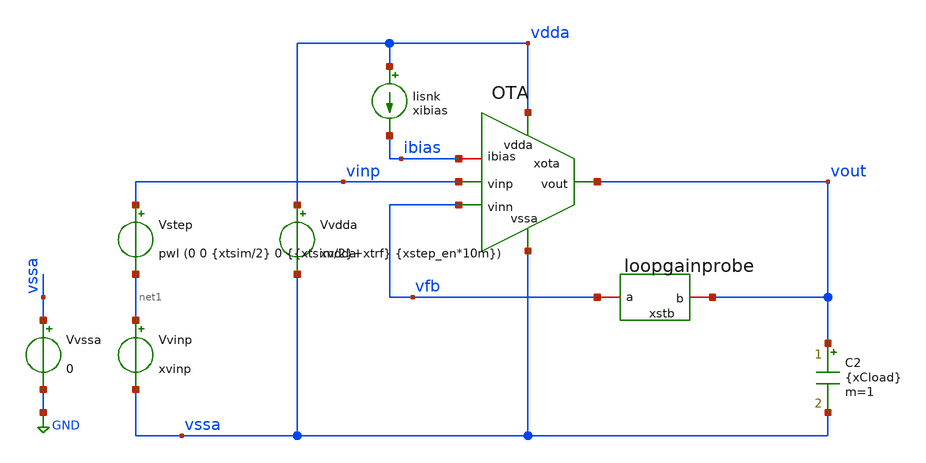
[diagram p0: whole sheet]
** sch_path: Questions/PVT_runs/tb_OTA_PVT.sch
**.subckt tb_OTA_PVT
Vvdda vdda vssa xvdda
Iisnk vdda ibias xibias
C2 vout vssa {xCload} m=1
xota vdda vinp vfb vssa vout ibias OTA
Vstep vinp net1 pwl (0 0 {xtsim/2} 0 {{xtsim/2}+xtrf} {xstep_en*10m})
Vvinp net1 vssa xvinp
Vvssa vssa GND 0
xstb vfb vout loopgainprobe
**** begin user architecture code

** opencircuitdesign pdks install
*.lib $::SKYWATER_MODELS/sky130.lib.spice tt
.lib /home/slice/pdk/SW130/share/pdk/sky130A/libs.tech/combined/sky130.lib.spice tt
*.lib /home/slice/pdk/SW130/share/pdk/sky130A/libs.tech/combined/sky130.lib.spice ss
*.lib /home/slice/pdk/SW130/share/pdk/sky130A/libs.tech/combined/sky130.lib.spice ff
*.lib /home/slice/pdk/SW130/share/pdk/sky130A/libs.tech/combined/sky130.lib.spice sf
*.lib /home/slice/pdk/SW130/share/pdk/sky130A/libs.tech/combined/sky130.lib.spice fs

* Parameters
.param xvdda = 1.8
.param xvinp = 1
.param xibias = 2u
.param xCload = 2p
.param xgm_dp = 1e-3
.param xRin = 1/xgm_dp
.param xCout = 1p
.param xRout = 1e6
.param xtrf = 50p
* need to set this equal to xtsim in the .control statement
.param xtsim = 50u
*.param xtsim = 1m
.csparam xtsim_var = 'xtsim'
.param xstep_en = 1
.temp 27
*.set csnumprec=2


  .control

  *let xtsim_var = 50u
  *let xtsim_var = 1m
  save all
   echo $&xtsim_var
*.csparam xtsim_var = 50u
** 1. TRAN ANALYSIS **

  tran 1n $&xtsim_var
  *tran 1n xtsim_var
  remzerovec
  write tb_OTA_PVT_tran.raw

** 2. AC ANALYSIS **

  alter i.xstb.Ii acmag=0
  alter v.xstb.Vi acmag=1

  ac dec 10 1 100G
  remzerovec
  write tb_OTA_PVT_ac1.raw

  alter i.xstb.Ii acmag=1
  alter v.xstb.Vi acmag=0
  ac dec 10 1 100G
  * use this line if you want the phase response to start at 0deg (more conventional and directly
+ corresponds to Franks derivation)
  * also the measures assume phase starts at 0deg
  let av = {1/(1/(2*(ac1.i(v.xstb.Vi)*ac2.v(xstb.x)-ac1.v(xstb.x)*ac2.i(v.xstb.Vi))+ac1.v(xstb.x)+ac2.i(v.xstb.Vi))-1)}
  remzerovec
  write tb_OTA_PVT_ac2.raw

  ** 3. MEASURES **

  * I am using octave to summarise all ac_measures files into a csv file which is then read by
+ loffice. loffice (mostly!) rounds to 3 decimal
  * places which I can't seem to change. Therefore, ngspice needs to output to 3 decimal places in order for the user to be able to
  * find a measurement, shown in the loffice csv summary, in the original raw files (to determine corner run). If the numbers are
  * > 10 you need csnumprec = 5 (5 digits means 10 and 3 decimal places). If the numbers are < 10 set csmnumprec = 4 and if numbers
  * are > 100, set csmnumprec = 6. This is why before I write the measure to the output txt file I check if it is < 10 / >=10 / >= 100
  * and set csmnumprec accordingly

  * 3.1 DC gain (Av_0):
  meas AC Av_0 FIND vdb(av) AT=1
  if $&Av_0 < 10
  set csnumprec=4
  end
  if $&Av_0 >= 10
  set csnumprec=5
  end
  if $&Av_0 >= 100
  set csnumprec=6
  end
  echo "$&Av_0" > ac_measures.txt
  echo --

  * 3.2 Bandwidth (BW):
  let n45_rads = -45*(pi/180)
  meas AC BW WHEN vp(av)=n45_rads CROSS=1
  let BW_kHz = BW/1e3
  if $&BW_kHz < 10
  set csnumprec=4
  end
  if $&BW_kHz >= 10
  set csnumprec=5
  end
  if $&BW_kHz >= 100
  set csnumprec=6
  end
  echo "$&BW_kHz" >> ac_measures.txt
  echo --

  * 3.3 Av at BW (Av_BW):
  *I am leaving this in for infomation but typically dont use it
  *meas AC Av_BW FIND vdb(av) WHEN vp(av)=n45_rads CROSS=1
  *echo "$&Av_BW" >> ac_measures.txt
  *echo --

  * 3.4 Unity loop gain frequency (ULGF):
  meas AC ULGF WHEN vdb(av)=0
  let ULGF_MHz = ULGF/1e6
  if $&ULGF_MHz < 10
  set csnumprec=4
  end
  if $&ULGF_MHz >= 10
  set csnumprec=5
  end
  if $&ULGF_MHz >= 100
  set csnumprec=6
  end
  echo "$&ULGF_MHz" >> ac_measures.txt
  echo --

  * 3.5 Phase margin (PM):
  meas AC ULGF_phi_rads FIND vp(av) WHEN vdb(av)=0 CROSS=1
  let ULGF_phi_deg = ULGF_phi_rads*(180/pi)
  let PM = 180+ULGF_phi_deg
  if $&PM < 10
  set csnumprec=4
  end
  if $&PM >= 10
  set csnumprec=5
  end
  if $&PM >= 100
  set csnumprec=6
  end
  echo "$&PM" >> ac_measures.txt
  echo --

  * 3.6 Gain margin (GM):
  * putting in -179 since a purely 2nd-order system so doesnt ever achieve -180
  * will prob revisit this later and change to 180
  let n180_rads = -179*(pi/180)
  meas AC GM FIND vdb(av) WHEN vp(av)=n180_rads CROSS=1
  * Note: The no of significant digits increases by 1 to include the - sign
  if $&GM < 10
  set csnumprec=5
  end
  if $&GM >= 10
  set csnumprec=6
  end
  if $&GM >= 100
  set csnumprec=7
  end
  echo "$&GM" >> ac_measures.txt
  echo --

  setplot

quit 0
.endc




**** end user architecture code
**.ends
.GLOBAL GND
.end
